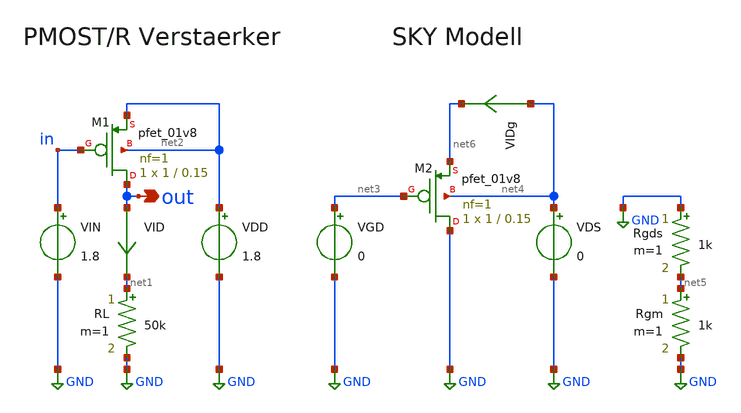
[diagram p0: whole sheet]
** sch_path: designs/a1_k12136610.sch
**.subckt a1_k12136610 out
*.opin out
XM1 out in net2 net2 sky130_fd_pr__pfet_01v8 L=0.15 W=1 nf=1 ad='int((1 + 1)/2) * 1 / 1 * 0.29' as='int((1 + 2)/2) * 1 / 1 * 0.29'
+ pd='2*int((1 + 1)/2) * (1 / 1 + 0.29)' ps='2*int((1 + 2)/2) * (1 / 1 + 0.29)' nrd='0.29 / 1 ' nrs='0.29 / 1 '
+ sa=0 sb=0 sd=0 mult=1 m=1
VIN in GND 1.8
VDD net2 GND 1.8
RL net1 GND 50k m=1
XM2 GND net3 net6 net4 sky130_fd_pr__pfet_01v8 L=0.15 W=1 nf=1 ad='int((1 + 1)/2) * 1 / 1 * 0.29' as='int((1 + 2)/2) * 1 / 1 * 0.29'
+ pd='2*int((1 + 1)/2) * (1 / 1 + 0.29)' ps='2*int((1 + 2)/2) * (1 / 1 + 0.29)' nrd='0.29 / 1 ' nrs='0.29 / 1 '
+ sa=0 sb=0 sd=0 mult=1 m=1
VGD net3 GND 0
VDS net4 GND 0
Rgds GND net5 1k m=1
Rgm net5 GND 1k m=1
VIDg net4 net6 0
.save i(vidg)
VID out net1 0
.save i(vid)
**** begin user architecture code


.lib /foss/pdks/sky130A/libs.tech/ngspice/sky130.lib.spice tt

.control
set xbrushwidth=7
set xgridwidth=2
set xfont_size=20

alter @RL[resistance]=50k

dc VIN 0 1.8 1m
let A0=deriv(-out)
plot out
plot A0
meas DC A0max max A0
meas DC vgd_op max_at A0
meas DC vds_op find out at=vgd_op

alter @VGD[dc]=vgd_op
alter @VDS[dc]=vds_op

dc VDS 0 1.8 1m
let func_gds=deriv(I(VIDg))
plot func_gds
meas DC gds find func_gds at=@VDS[dc]
alter @Rgds[resistance]=1/gds

dc VGD 0 1.8 1m
let func_gm=deriv(I(VIDg))
plot func_gm
meas DC gm find func_gm at=@VGD[dc]
alter @Rgm[resistance]=1/gm

let A0_calc=1/(@Rgm[resistance]*(1/@Rgds[resistance]+1/@RL[resistance]))
print A0_calc

.endc
.save all


**** end user architecture code
**.ends
.GLOBAL GND
.end
